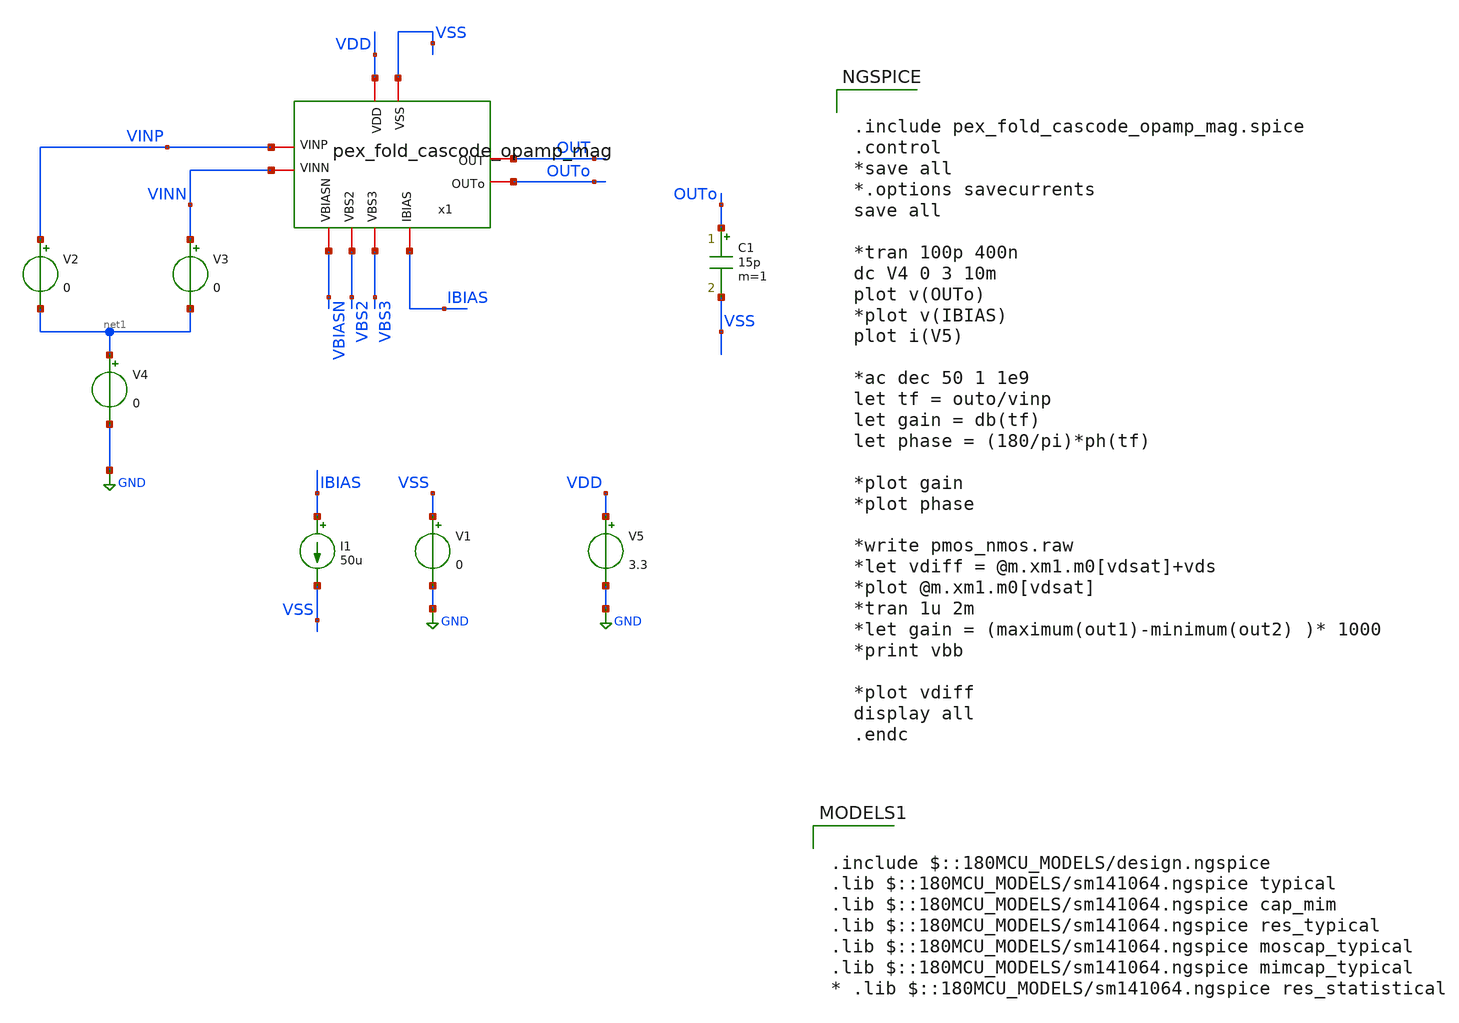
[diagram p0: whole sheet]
** sch_path: SCOP_INPUT_AND_MUX_PAKISTAN_03/Xschem/Folded_single/folded_single_TB_DC.sch
**.subckt folded_single_TB_DC
V5 VDD GND 3.3
V2 VINP net1 0
V1 VSS GND 0
I1 IBIAS VSS 50u
C1 OUTo VSS 15p m=1
V3 VINN net1 0
x1 OUT VDD VSS VINN VINP IBIAS VBS2 VBS3 VBIASN OUTo pex_fold_cascode_opamp_mag
V4 net1 GND 0
**** begin user architecture code


.include pex_fold_cascode_opamp_mag.spice
.control
*save all
*.options savecurrents
save all

*tran 100p 400n
dc V4 0 3 10m
plot v(OUTo)
*plot v(IBIAS)
plot i(V5)

*ac dec 50 1 1e9
let tf = outo/vinp
let gain = db(tf)
let phase = (180/pi)*ph(tf)

*plot gain
*plot phase

*write pmos_nmos.raw
*let vdiff = @m.xm1.m0[vdsat]+vds
*plot @m.xm1.m0[vdsat]
*tran 1u 2m
*let gain = (maximum(out1)-minimum(out2) )* 1000
*print vbb

*plot vdiff
display all
.endc



.include $::180MCU_MODELS/design.ngspice
.lib $::180MCU_MODELS/sm141064.ngspice typical
.lib $::180MCU_MODELS/sm141064.ngspice cap_mim
.lib $::180MCU_MODELS/sm141064.ngspice res_typical
.lib $::180MCU_MODELS/sm141064.ngspice moscap_typical
.lib $::180MCU_MODELS/sm141064.ngspice mimcap_typical
* .lib $::180MCU_MODELS/sm141064.ngspice res_statistical

**** end user architecture code
**.ends
.GLOBAL GND
.end
